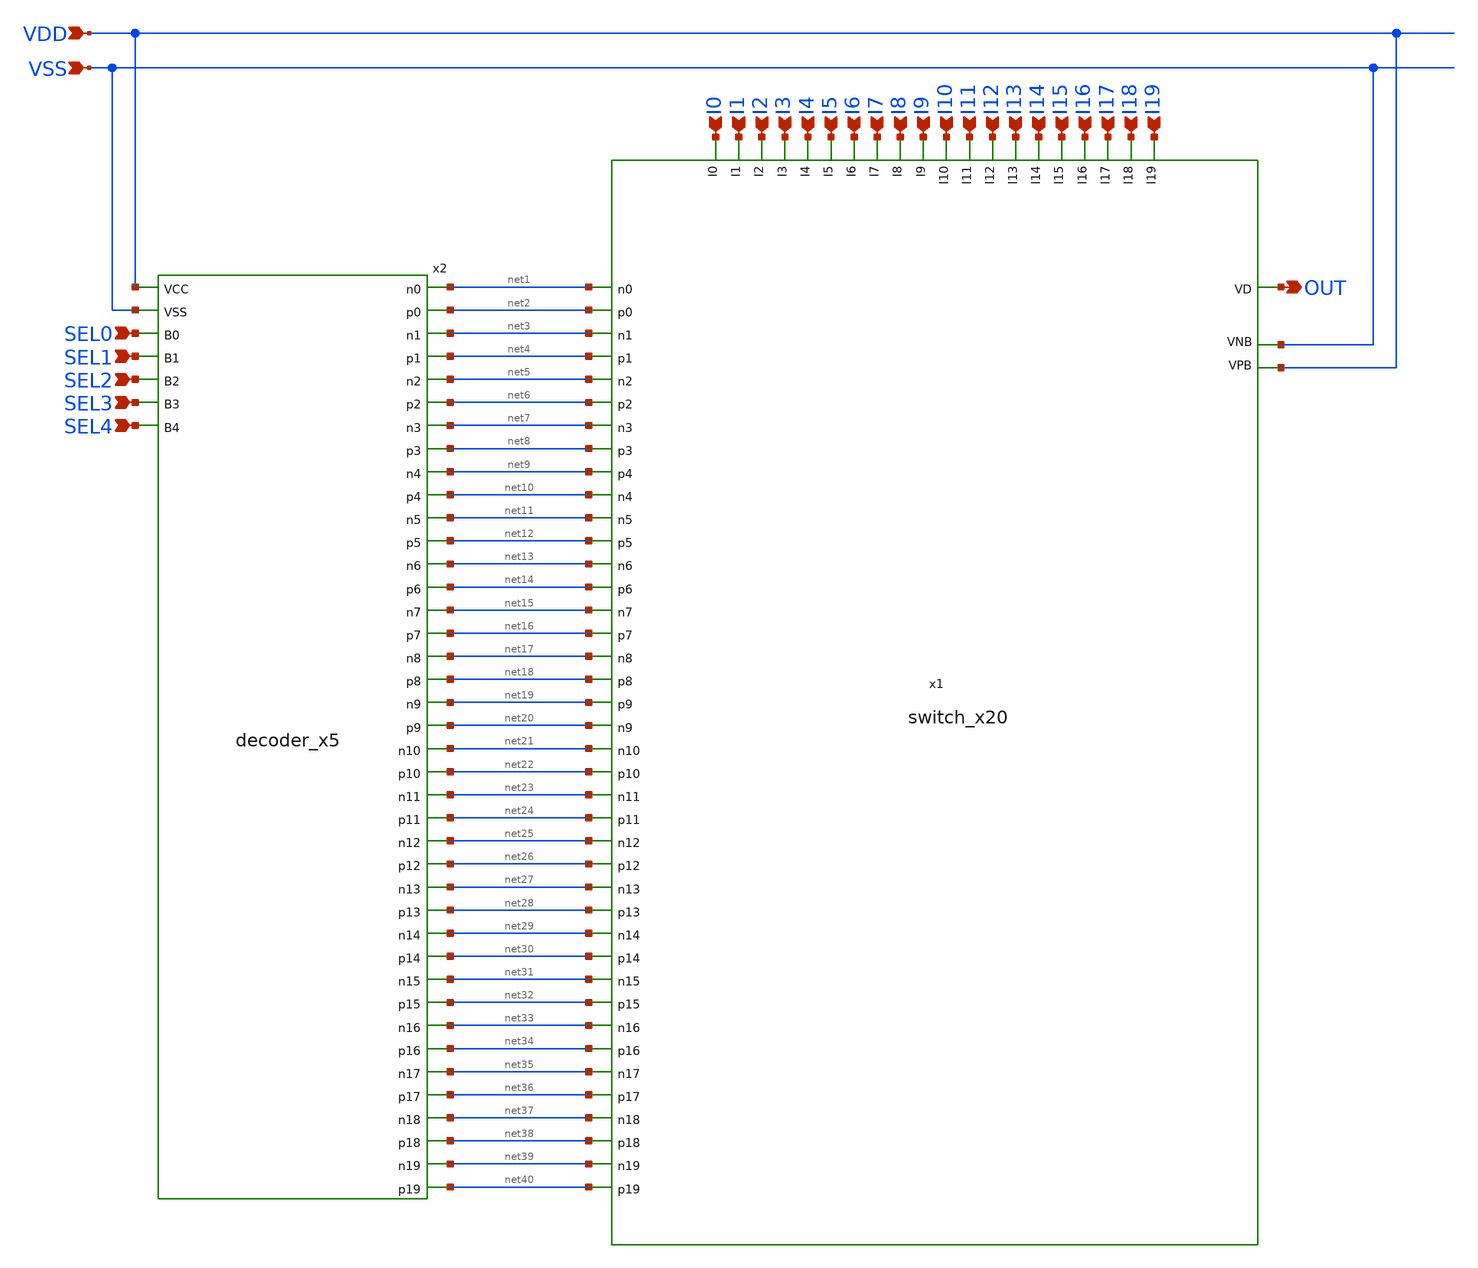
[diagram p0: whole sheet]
** sch_path: analog/library/AnalogMux/schematics/analog_mux.sch
**.subckt analog_mux I0 I1 I2 I3 I4 I5 I6 I7 I8 I9 I10 I11 I12 I13 I14 I15 I16 I17 I18 I19 OUT SEL0
*+ SEL1 SEL2 SEL3 SEL4 VDD VSS
*.ipin I0
*.ipin I1
*.ipin I2
*.ipin I3
*.ipin I4
*.ipin I5
*.ipin I6
*.ipin I7
*.ipin I8
*.ipin I9
*.ipin I10
*.ipin I11
*.ipin I12
*.ipin I13
*.ipin I14
*.ipin I15
*.ipin I16
*.ipin I17
*.ipin I18
*.ipin I19
*.opin OUT
*.ipin SEL0
*.ipin SEL1
*.ipin SEL2
*.ipin SEL3
*.ipin SEL4
*.ipin VDD
*.ipin VSS
x1 VDD VSS I0 net2 I2 net3 I1 net9 net5 net6 I6 net7 net8 I3 I9 net19 I4 net11 net12 I5 net13 net14
+ I14 net15 net16 I7 net17 net18 I8 net20 net10 net4 net21 net22 I10 net23 net24 I11 net25 net26 I12
+ net27 net28 I13 net29 net30 net1 net31 net32 I15 net33 net34 I16 net35 net36 I17 net37 net38 I18 net39
+ net40 I19 OUT switch_x20
x2 VDD VSS net15 net3 net39 net17 net31 net35 net37 net27 net7 net21 net19 net5 net25 net1 net33
+ net11 net13 net29 net23 net9 net24 net22 net8 net20 net18 net6 net2 net40 net38 net16 net36 net34 net14
+ net32 net30 net12 net28 net26 net10 net4 SEL0 SEL1 SEL2 SEL3 SEL4 decoder_x5
**.ends
.end
